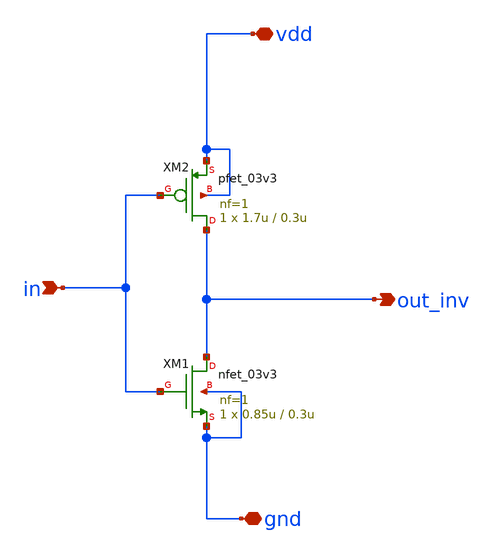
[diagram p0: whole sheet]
** sch_path: designs/libs/core_fpga/mux2x1_transmission_gate/mux_inverter.sch
**.subckt mux_inverter vdd gnd out_inv in
*.iopin vdd
*.iopin gnd
*.opin out_inv
*.ipin in
XM1 out_inv in gnd gnd nfet_03v3 L=0.3u W=0.85u nf=1 ad='int((nf+1)/2) * W/nf * 0.18u' as='int((nf+2)/2) * W/nf * 0.18u'
+ pd='2*int((nf+1)/2) * (W/nf + 0.18u)' ps='2*int((nf+2)/2) * (W/nf + 0.18u)' nrd='0.18u / W' nrs='0.18u / W'
+ sa=0 sb=0 sd=0 m=1
XM2 out_inv in vdd vdd pfet_03v3 L=0.3u W=1.7u nf=1 ad='int((nf+1)/2) * W/nf * 0.18u' as='int((nf+2)/2) * W/nf * 0.18u'
+ pd='2*int((nf+1)/2) * (W/nf + 0.18u)' ps='2*int((nf+2)/2) * (W/nf + 0.18u)' nrd='0.18u / W' nrs='0.18u / W'
+ sa=0 sb=0 sd=0 m=1
**.ends
.end
